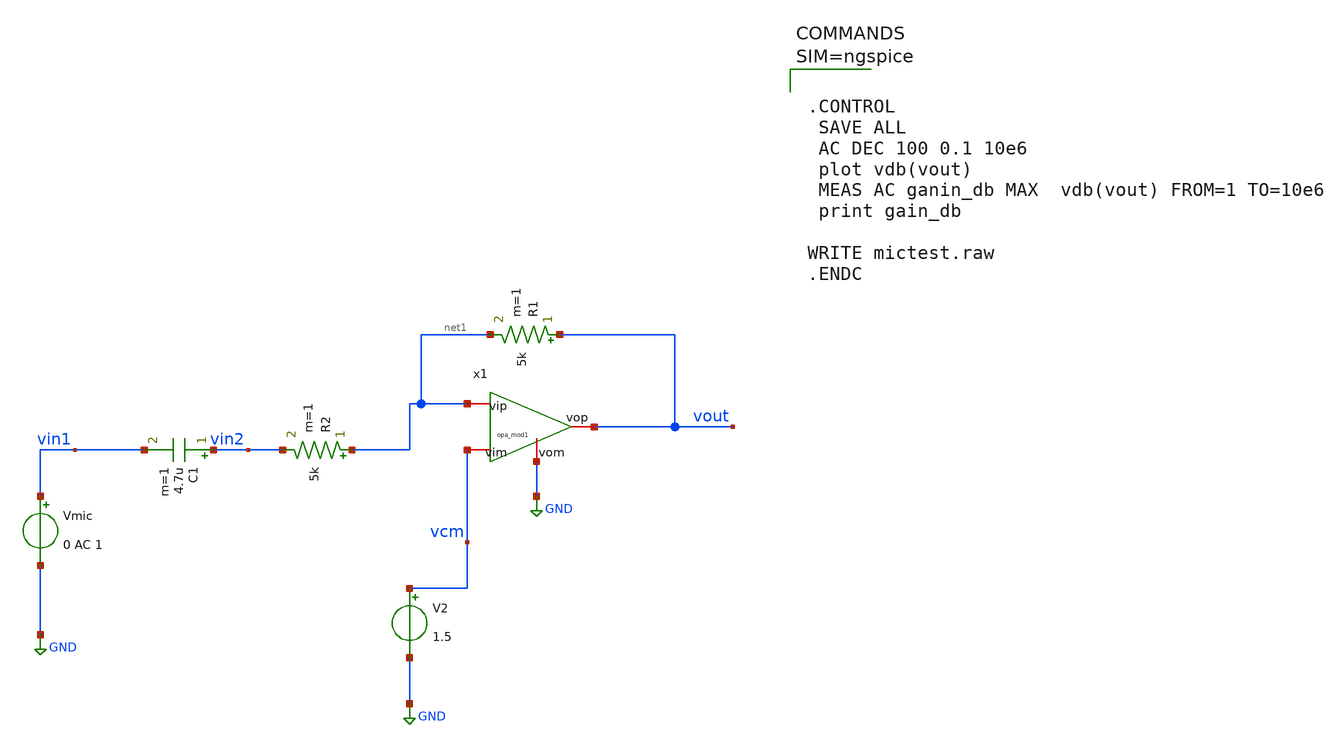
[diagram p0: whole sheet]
** sch_path: xschem/highpass_op.sch
**.subckt highpass_op
x1 vout net1 vcm GND opa_mod1
Vmic vin1 GND 0 AC 1
C1 vin2 vin1 4.7u m=1
R2 net1 vin2 5k m=1
R1 vout net1 5k m=1
V2 vcm GND 1.5
**** begin user architecture code



.CONTROL
 SAVE ALL
 AC DEC 100 0.1 10e6
 plot vdb(vout)
 MEAS AC ganin_db MAX  vdb(vout) FROM=1 TO=10e6
 print gain_db

WRITE mictest.raw
.ENDC



**** end user architecture code
**.ends
.GLOBAL GND
.end
